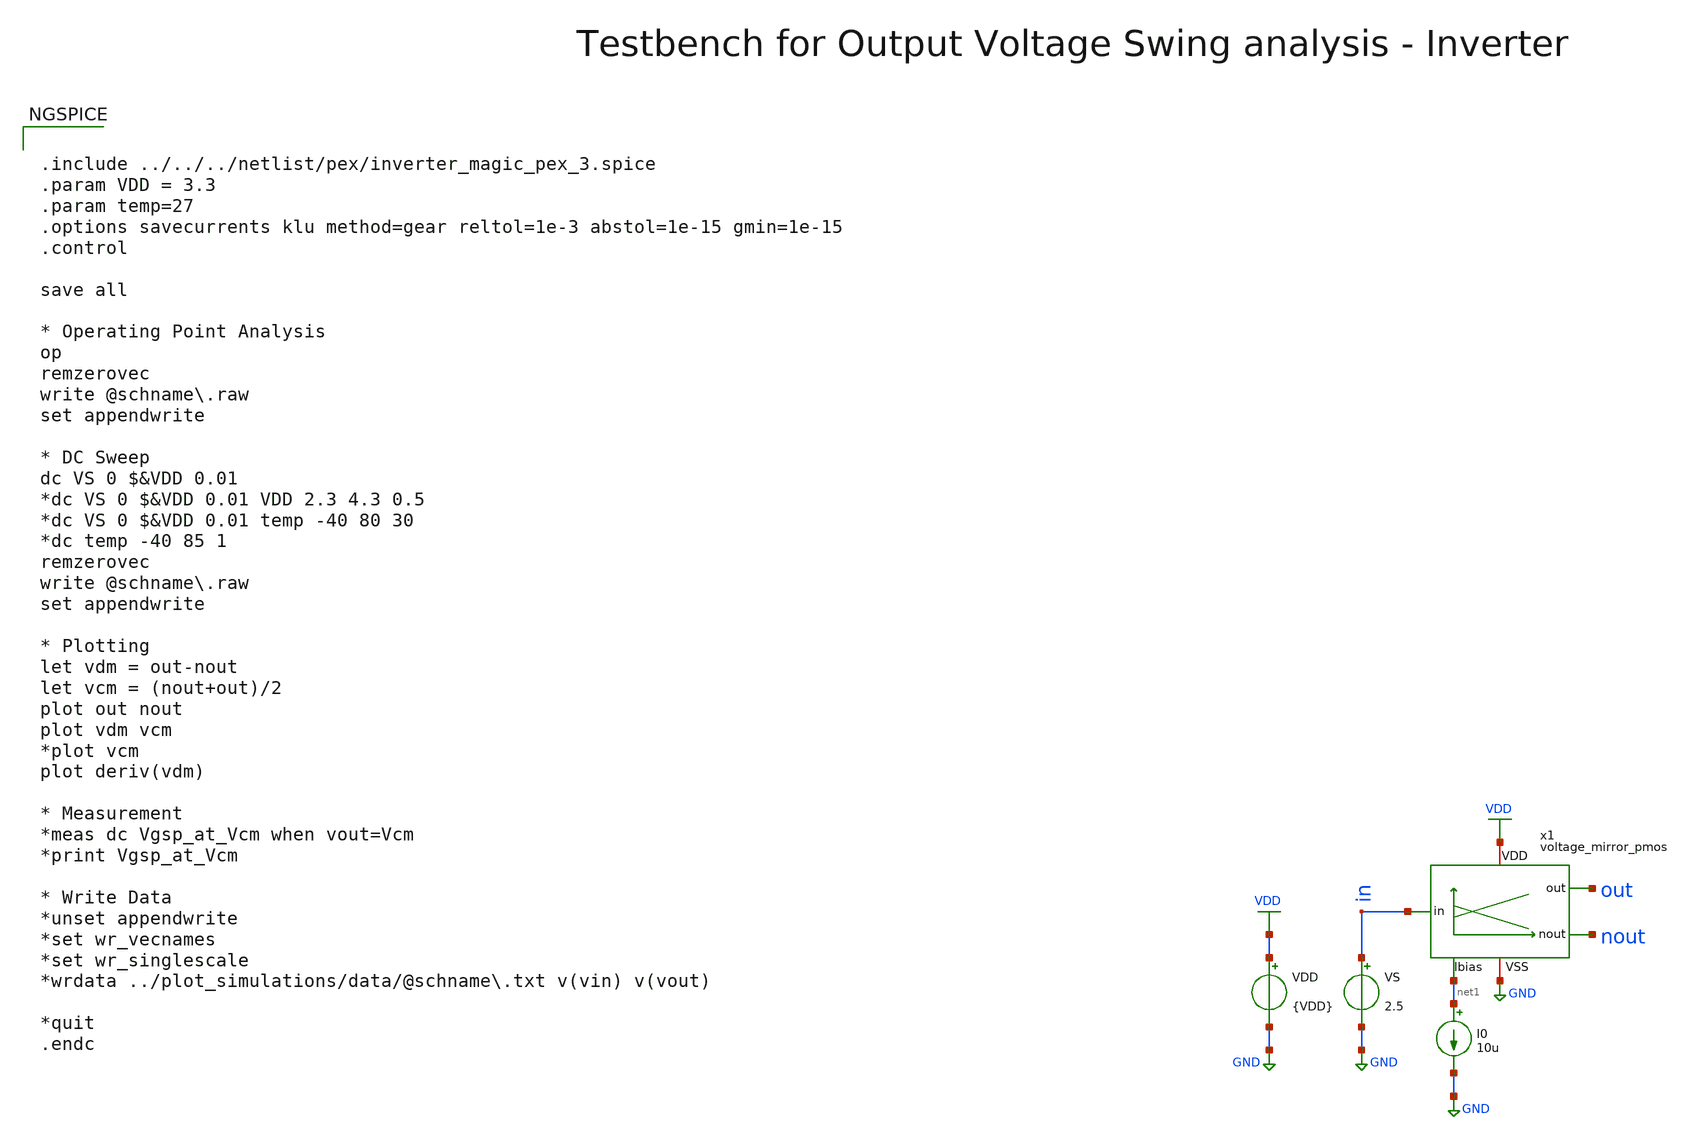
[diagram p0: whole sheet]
** sch_path: macros/heichips26_vcr/macros/switched_capacitor/testbenches/xschem/tb_voltage_mirror_pmos_dc.sch
**.subckt tb_voltage_mirror_pmos_dc
VDD VDD GND {VDD}
VS in GND 2.5
I0 net1 GND 10u
x1 net1 nout VDD in GND out voltage_mirror_pmos
**** begin user architecture code


.include ../../../netlist/pex/inverter_magic_pex_3.spice
.param VDD = 3.3
.param temp=27
.options savecurrents klu method=gear reltol=1e-3 abstol=1e-15 gmin=1e-15
.control

save all

* Operating Point Analysis
op
remzerovec
write @schname\.raw
set appendwrite

* DC Sweep
dc VS 0 $&VDD 0.01
*dc VS 0 $&VDD 0.01 VDD 2.3 4.3 0.5
*dc VS 0 $&VDD 0.01 temp -40 80 30
*dc temp -40 85 1
remzerovec
write @schname\.raw
set appendwrite

* Plotting
let vdm = out-nout
let vcm = (nout+out)/2
plot out nout
plot vdm vcm
*plot vcm
plot deriv(vdm)

* Measurement
*meas dc Vgsp_at_Vcm when vout=Vcm
*print Vgsp_at_Vcm

* Write Data
*unset appendwrite
*set wr_vecnames
*set wr_singlescale
*wrdata ../plot_simulations/data/@schname\.txt v(vin) v(vout)

*quit
.endc



.lib cornerMOSlv.lib mos_tt
.lib cornerMOShv.lib mos_tt
.lib cornerRES.lib res_typ
.lib cornerDIO.lib dio_tt

**** end user architecture code
**.ends

* expanding   symbol:  voltage_mirror_pmos.sym # of pins=6
** sym_path: macros/heichips26_vcr/macros/switched_capacitor/schematic/xschem/voltage_mirror_pmos.sym
** sch_path: macros/heichips26_vcr/macros/switched_capacitor/schematic/xschem/voltage_mirror_pmos.sch
.subckt voltage_mirror_pmos Ibias nout VDD in VSS out
*.iopin VDD
*.iopin VSS
*.ipin in
*.opin out
*.opin nout
*.ipin Ibias
**** begin user architecture code


.param n_w = 6u
.param n_l = 5u
.param p_w = 10u
.param p_l = 2u


**** end user architecture code
XR1 in Ibias VSS rhigh w=0.5e-6 l=34e-6 m=1 b=0 mm_ok=1
XM4 net1 Ibias VDD VDD sg13_hv_pmos w=p_w l=p_l ng=1 m=1 mm_ok=1
XM5 out net1 VSS VSS sg13_hv_nmos w=n_w l=n_l ng=1 m=1 mm_ok=1
XR2 VSS nout VSS rhigh w=0.5e-6 l=34e-6 m=1 b=0 mm_ok=1
XR3 out VDD VSS rhigh w=0.5e-6 l=34e-6 m=1 b=0 mm_ok=1
XM2 net1 net1 VSS VSS sg13_hv_nmos w=n_w l=n_l ng=1 m=1 mm_ok=1
XM3 nout Ibias VDD VDD sg13_hv_pmos w=p_w l=p_l ng=1 m=1 mm_ok=1
XM6 Ibias Ibias VDD VDD sg13_hv_pmos w=1.9*p_w l=p_l ng=1 m=1 mm_ok=1
.ends

.GLOBAL GND
.GLOBAL VDD
.end
